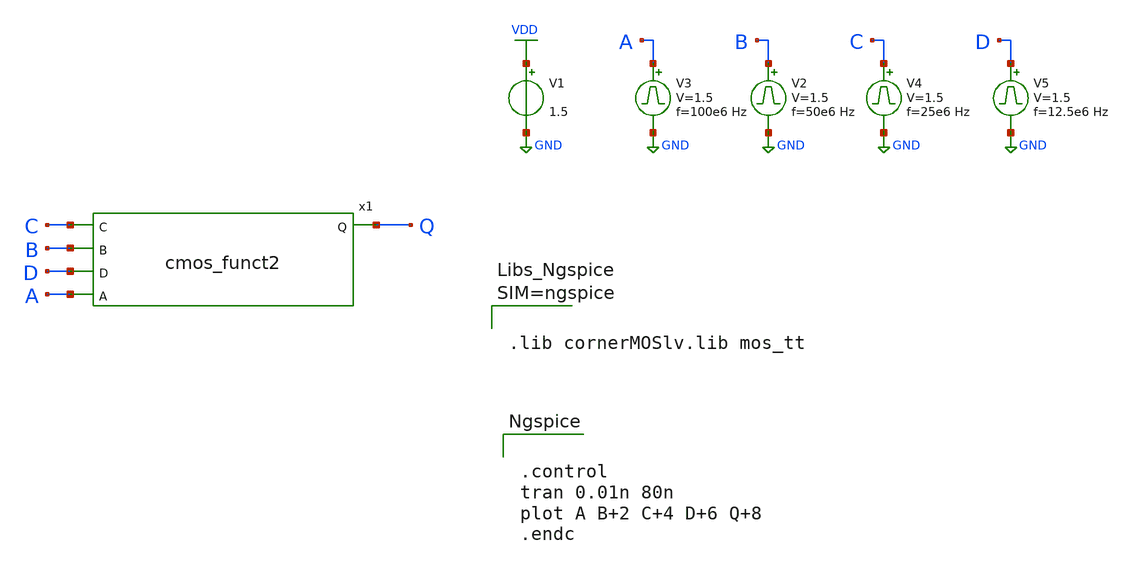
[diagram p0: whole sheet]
** sch_path: Modulo_Digital/Lab1/cmos_funct2_tb.sch
**.subckt cmos_funct2_tb
V1 VDD GND 1.5
V3 A GND pulse 0 1.5 '0.495/ 100e6 ' '0.01/100e6 ' '0.01/100e6 ' '0.49/100e6 ' '1/100e6 '
V2 B GND pulse 0 1.5 '0.495/ 50e6 ' '0.01/50e6 ' '0.01/50e6 ' '0.49/50e6 ' '1/50e6 '
V4 C GND pulse 0 1.5 '0.495/ 25e6 ' '0.01/25e6 ' '0.01/25e6 ' '0.49/25e6 ' '1/25e6 '
V5 D GND pulse 0 1.5 '0.495/ 12.5e6 ' '0.01/12.5e6 ' '0.01/12.5e6 ' '0.49/12.5e6 ' '1/12.5e6 '
x1 C B D A Q cmos_funct2
**** begin user architecture code


.control
tran 0.01n 80n
plot A B+2 C+4 D+6 Q+8
.endc




.lib cornerMOSlv.lib mos_tt



**** end user architecture code
**.ends

* expanding   symbol:  cmos_funct2.sym # of pins=5
** sym_path: Modulo_Digital/Lab1/cmos_funct2.sym
** sch_path: Modulo_Digital/Lab1/cmos_funct2.sch
.subckt cmos_funct2 C B D A Q
*.opin Q
*.ipin B
*.ipin C
*.ipin D
*.ipin A
XM1 net1 C VDD VDD sg13_lv_pmos w=1u l=0.13u ng=1 m=1 mm_ok=1
XM2 net2 B VDD VDD sg13_lv_pmos w=1u l=0.13u ng=1 m=1 mm_ok=1
XM3 net2 D net1 VDD sg13_lv_pmos w=1u l=0.13u ng=1 m=1 mm_ok=1
XM4 Q A net2 VDD sg13_lv_pmos w=1u l=0.13u ng=1 m=1 mm_ok=1
XM5 Q B net3 GND sg13_lv_nmos w=1u l=0.13u ng=1 m=1 mm_ok=1
XM6 Q A GND GND sg13_lv_nmos w=1u l=0.13u ng=1 m=1 mm_ok=1
XM7 net3 C GND GND sg13_lv_nmos w=1u l=0.13u ng=1 m=1 mm_ok=1
XM8 net3 D GND GND sg13_lv_nmos w=1u l=0.13u ng=1 m=1 mm_ok=1
.ends

.GLOBAL VDD
.GLOBAL GND
.end
